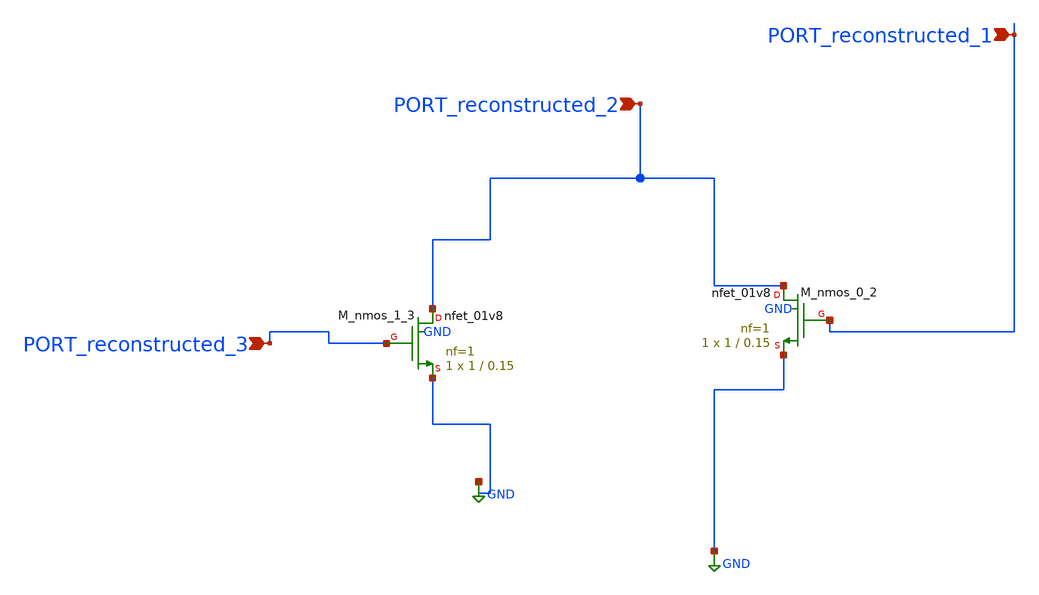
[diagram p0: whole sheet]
** sch_path: schematics/AMSNet/664.sch
**.subckt 664 PORT_reconstructed_3 PORT_reconstructed_2 PORT_reconstructed_1
*.ipin PORT_reconstructed_3
*.ipin PORT_reconstructed_2
*.ipin PORT_reconstructed_1
XM_nmos_0_2 PORT_reconstructed_2 PORT_reconstructed_1 GND GND sky130_fd_pr__nfet_01v8 L=0.15 W=1 nf=1
+ ad='int((1 + 1)/2) * 1 / 1 * 0.29' as='int((1 + 2)/2) * 1 / 1 * 0.29' pd='2*int((1 + 1)/2) * (1 / 1 + 0.29)'
+ ps='2*int((1 + 2)/2) * (1 / 1 + 0.29)' nrd='0.29 / 1 ' nrs='0.29 / 1 ' sa=0 sb=0 sd=0 mult=1 m=1
XM_nmos_1_3 PORT_reconstructed_2 PORT_reconstructed_3 GND GND sky130_fd_pr__nfet_01v8 L=0.15 W=1 nf=1
+ ad='int((1 + 1)/2) * 1 / 1 * 0.29' as='int((1 + 2)/2) * 1 / 1 * 0.29' pd='2*int((1 + 1)/2) * (1 / 1 + 0.29)'
+ ps='2*int((1 + 2)/2) * (1 / 1 + 0.29)' nrd='0.29 / 1 ' nrs='0.29 / 1 ' sa=0 sb=0 sd=0 mult=1 m=1
**.ends
.GLOBAL GND
.end
